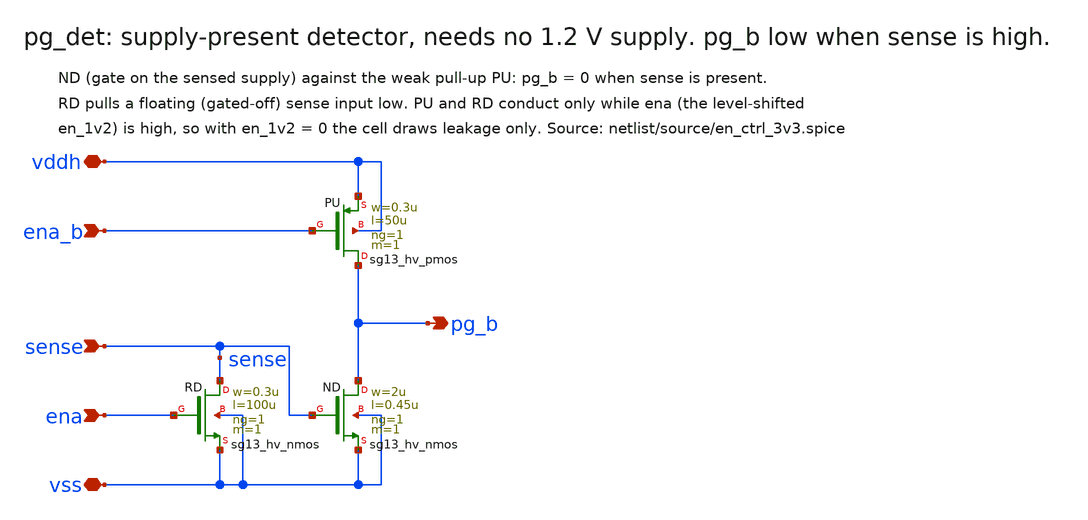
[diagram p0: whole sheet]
** sch_path: macros/en_ctrl_3v3/schematic/xschem/pg_det.sch
**.subckt pg_det vddh vss sense pg_b ena ena_b
*.iopin vddh
*.iopin vss
*.ipin sense
*.opin pg_b
*.ipin ena
*.ipin ena_b
XPU pg_b ena_b vddh vddh sg13_hv_pmos w=0.3u l=50u ng=1 m=1 mm_ok=1
XND pg_b sense vss vss sg13_hv_nmos w=2u l=0.45u ng=1 m=1 mm_ok=1
XRD sense ena vss vss sg13_hv_nmos w=0.3u l=100u ng=1 m=1 mm_ok=1
**.ends
.end
